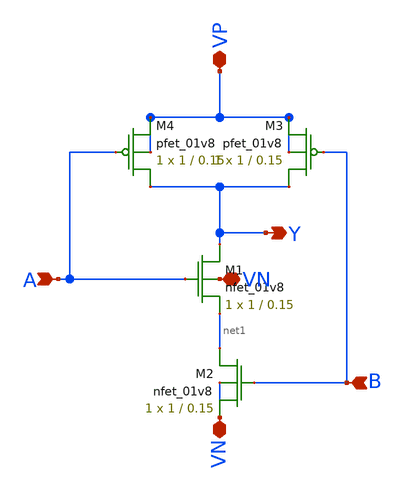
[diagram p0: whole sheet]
** sch_path: mini1/NAND2.sch
**.subckt NAND2 A B VN VP VN Y
*.ipin A
*.ipin B
*.iopin VN
*.iopin VP
*.iopin VN
*.opin Y
XM1 Y A net1 VN sky130_fd_pr__nfet_01v8 L=0.15 W=1 nf=1 ad='int((nf+1)/2) * W/nf * 0.29' as='int((nf+2)/2) * W/nf * 0.29'
+ pd='2*int((nf+1)/2) * (W/nf + 0.29)' ps='2*int((nf+2)/2) * (W/nf + 0.29)' nrd='0.29 / W' nrs='0.29 / W'
+ sa=0 sb=0 sd=0 mult=1 m=1
XM2 net1 B VN VN sky130_fd_pr__nfet_01v8 L=0.15 W=1 nf=1 ad='int((nf+1)/2) * W/nf * 0.29' as='int((nf+2)/2) * W/nf * 0.29'
+ pd='2*int((nf+1)/2) * (W/nf + 0.29)' ps='2*int((nf+2)/2) * (W/nf + 0.29)' nrd='0.29 / W' nrs='0.29 / W'
+ sa=0 sb=0 sd=0 mult=1 m=1
XM3 Y B VP VP sky130_fd_pr__pfet_01v8 L=0.15 W=1 nf=1 ad='int((nf+1)/2) * W/nf * 0.29' as='int((nf+2)/2) * W/nf * 0.29'
+ pd='2*int((nf+1)/2) * (W/nf + 0.29)' ps='2*int((nf+2)/2) * (W/nf + 0.29)' nrd='0.29 / W' nrs='0.29 / W'
+ sa=0 sb=0 sd=0 mult=1 m=1
XM4 Y A VP VP sky130_fd_pr__pfet_01v8 L=0.15 W=1 nf=1 ad='int((nf+1)/2) * W/nf * 0.29' as='int((nf+2)/2) * W/nf * 0.29'
+ pd='2*int((nf+1)/2) * (W/nf + 0.29)' ps='2*int((nf+2)/2) * (W/nf + 0.29)' nrd='0.29 / W' nrs='0.29 / W'
+ sa=0 sb=0 sd=0 mult=1 m=1
**.ends
.end
